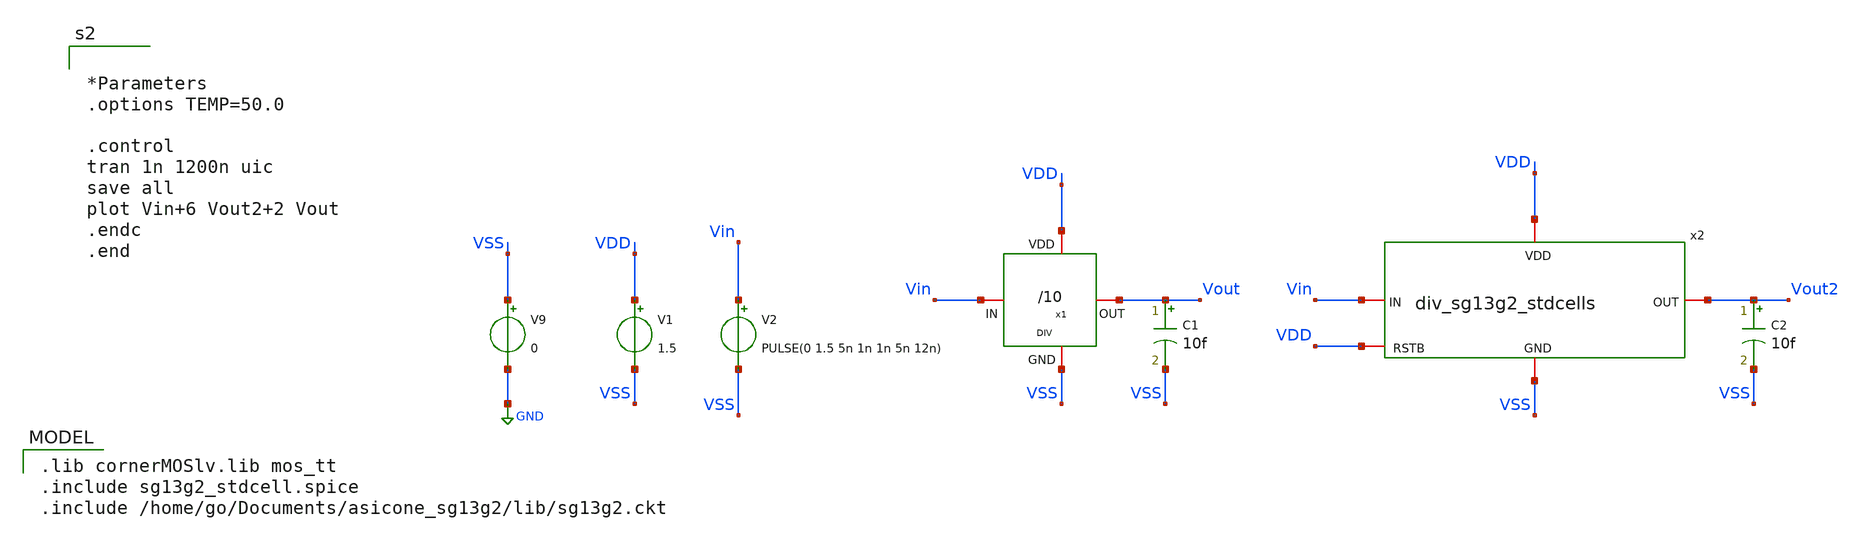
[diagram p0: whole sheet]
** sch_path: unic_cass_wrapper_user_project/ROs_reliability/divider_tb.sch
**.subckt divider_tb
x1 VDD Vout Vin VSS DIV
V9 VSS GND 0
V1 VDD VSS 1.5
V2 Vin VSS PULSE(0 1.5 5n 1n 1n 5n 12n)
C1 Vout VSS 10f m=1
x2 VDD Vout2 Vin VSS VDD div_sg13g2_stdcells
C2 Vout2 VSS 10f m=1
**** begin user architecture code
 .lib cornerMOSlv.lib mos_tt
.include sg13g2_stdcell.spice
.include /home/go/Documents/asicone_sg13g2/lib/sg13g2.ckt



*Parameters
.options TEMP=50.0

.control
tran 1n 1200n uic
save all
plot Vin+6 Vout2+2 Vout
.endc
.end


**** end user architecture code
**.ends
.GLOBAL GND
.end
